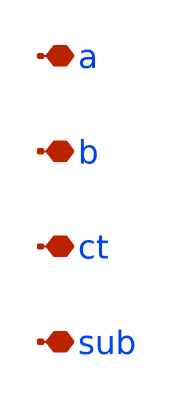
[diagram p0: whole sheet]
** sch_path: sch/inductor/inductor_ind_05_220.sch
**.subckt inductor_ind_05_220 a b ct sub
*.iopin a
*.iopin b
*.iopin ct
*.iopin sub
**** begin user architecture code


R31 net27 b r=1e-2
R26 a net23 r=1e-2
C2 net27 net31 c=223.7e-15
C24 net35 net27 c=205e-15
C25 net23 net37 c=223.7e-15
R5 sub net31 r=5.358e3
R4 net41 net27 r=2.059
R13 net23 net35 r=9.064
R10 sub net37 r=5.358e3
R9 net23 net39 r=2.059
L1 net39 ct l=4.96e-9
L3 ct net41 l=4.96e-9


**** end user architecture code
**.ends
.end
